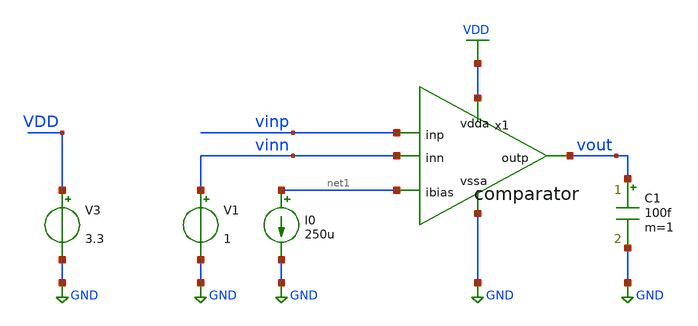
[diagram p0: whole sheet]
** sch_path: xschem/tb_comp_tran_vos_tt_mm.sch
**.subckt tb_comp_tran_vos_tt_mm
I0 net1 GND 250u
C1 vout GND 100f m=1
V1 vinn GND 1
V3 VDD GND 3.3
x1 VDD net1 vinp vinn vout GND comparator
**** begin user architecture code



.lib /home/ttuser/pdk/sky130A/libs.tech/ngspice/sky130.lib.spice tt_mm

*.option temp=27

vinsource vinp 0 pwl(0 0.9 1e-3 1.1 2e-3 0.9)

.control
  option seed=9
  let run=0
  let run_max=100
  let voff_new=vector(run_max+1)
  dowhile run <= run_max
    tran 0.1us 2ms
    let vdiff=v(vinp)-1
    meas tran voff_rise find vdiff when v(vout)=10e-3 rise=1
    meas tran voff_fall find vdiff when v(vout)=3.29 fall=1
    let voff_new[run]=(voff_rise+voff_fall)/2
    print voff_new
    print run
    save voff_new
    write voff_new.out voff_new
    *set appendwrite
    *write tran.out v(vout)
    reset
    let run=run+1
  end
  *plot tran1.v(vout) tran2.v(vout) tran3.v(vout) tran4.v(vout) tran5.v(vout)
  *+ tran6.v(vout) tran7.v(vout) tran8.v(vout) tran9.v(vout) tran10.v(vout)
  *+ tran11.v(vout) tran12.v(vout) tran13.v(vout) tran14.v(vout) tran15.v(vout)
  *+ tran16.v(vout) tran17.v(vout) tran18.v(vout) tran19.v(vout) tran20.v(vout)
  *+ tran21.v(vout) tran22.v(vout) tran23.v(vout) tran24.v(vout) tran25.v(vout)
  *+ tran26.v(vout) tran27.v(vout) tran28.v(vout) tran29.v(vout) tran30.v(vout)
  *+ tran31.v(vout) tran32.v(vout) tran33.v(vout) tran34.v(vout) tran35.v(vout)
  *+ tran36.v(vout) tran37.v(vout) tran38.v(vout) tran39.v(vout) tran40.v(vout)
  *+ tran41.v(vout) tran42.v(vout) tran43.v(vout) tran44.v(vout) tran45.v(vout)
  *+ tran46.v(vout) tran47.v(vout) tran48.v(vout) tran49.v(vout) tran50.v(vout)
  *+ v(vinp) v(vinn)
.endc



**** end user architecture code
**.ends
.GLOBAL GND
.GLOBAL VDD
.end
